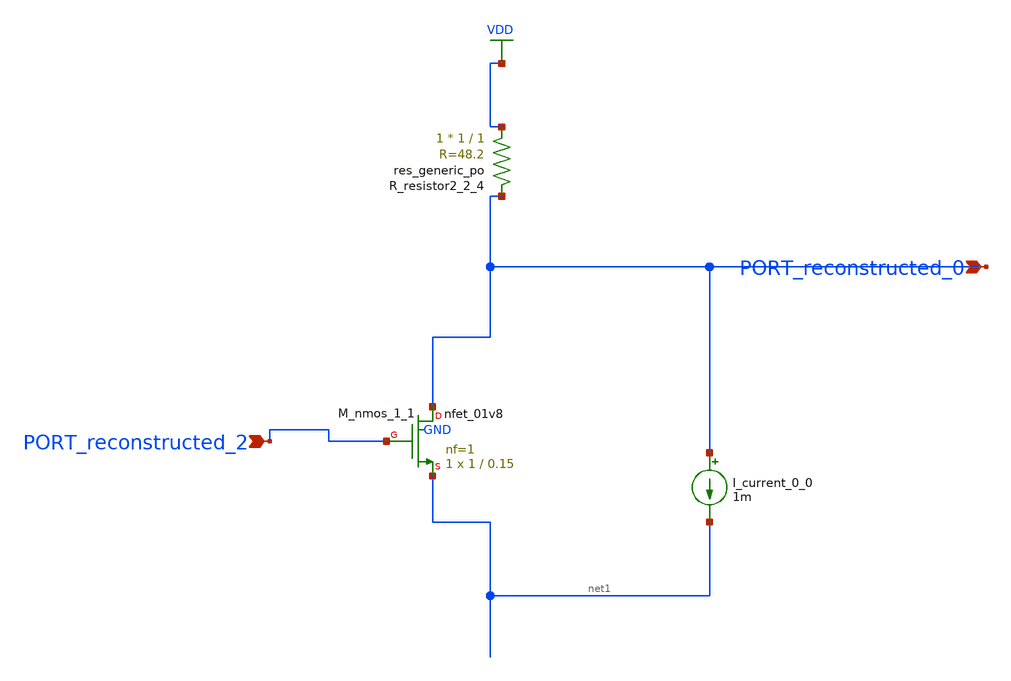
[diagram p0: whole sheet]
** sch_path: schematics/AMSNet/477.sch
**.subckt 477 PORT_reconstructed_2 PORT_reconstructed_0
*.ipin PORT_reconstructed_2
*.ipin PORT_reconstructed_0
I_current_0_0 PORT_reconstructed_0 net1 1m
XM_nmos_1_1 PORT_reconstructed_0 PORT_reconstructed_2 net1 GND sky130_fd_pr__nfet_01v8 L=0.15 W=1 nf=1
+ ad='int((1 + 1)/2) * 1 / 1 * 0.29' as='int((1 + 2)/2) * 1 / 1 * 0.29' pd='2*int((1 + 1)/2) * (1 / 1 + 0.29)'
+ ps='2*int((1 + 2)/2) * (1 / 1 + 0.29)' nrd='0.29 / 1 ' nrs='0.29 / 1 ' sa=0 sb=0 sd=0 mult=1 m=1
XR_resistor2_2_4 VDD PORT_reconstructed_0 sky130_fd_pr__res_generic_po W=1 L=1 m=1
**.ends
.GLOBAL VDD
.end
